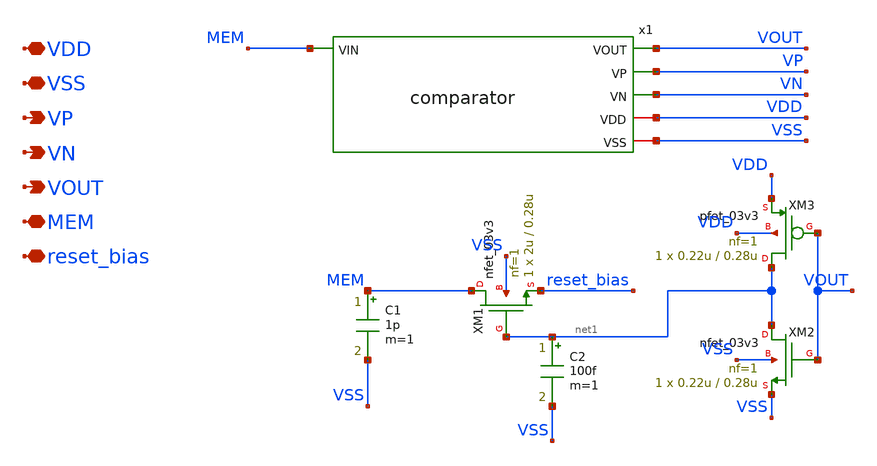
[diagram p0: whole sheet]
** sch_path: analog/neuron/neuron.sch
**.subckt neuron VDD VSS VP VN VOUT MEM reset_bias
*.iopin VDD
*.iopin VSS
*.opin VP
*.opin VN
*.opin VOUT
*.iopin MEM
*.iopin reset_bias
XM1 MEM net1 reset_bias VSS nfet_03v3 L=0.28u W=2u nf=1 ad='int((nf+1)/2) * W/nf * 0.18u' as='int((nf+2)/2) * W/nf * 0.18u'
+ pd='2*int((nf+1)/2) * (W/nf + 0.18u)' ps='2*int((nf+2)/2) * (W/nf + 0.18u)' nrd='0.18u / W' nrs='0.18u / W'
+ sa=0 sb=0 sd=0 m=1
C1 MEM VSS 1p m=1
x1 MEM VOUT VP VN VDD VSS comparator
XM2 net1 VOUT VSS VSS nfet_03v3 L=0.28u W=0.22u nf=1 ad='int((nf+1)/2) * W/nf * 0.18u' as='int((nf+2)/2) * W/nf * 0.18u'
+ pd='2*int((nf+1)/2) * (W/nf + 0.18u)' ps='2*int((nf+2)/2) * (W/nf + 0.18u)' nrd='0.18u / W' nrs='0.18u / W'
+ sa=0 sb=0 sd=0 m=1
XM3 net1 VOUT VDD VDD pfet_03v3 L=0.28u W=0.22u nf=1 ad='int((nf+1)/2) * W/nf * 0.18u' as='int((nf+2)/2) * W/nf * 0.18u'
+ pd='2*int((nf+1)/2) * (W/nf + 0.18u)' ps='2*int((nf+2)/2) * (W/nf + 0.18u)' nrd='0.18u / W' nrs='0.18u / W'
+ sa=0 sb=0 sd=0 m=1
C2 net1 VSS 100f m=1
**.ends
.end
